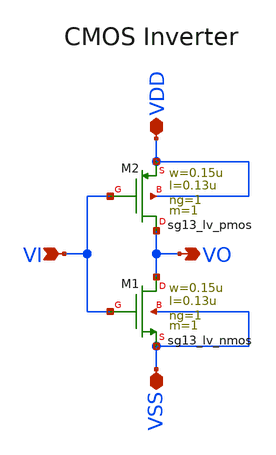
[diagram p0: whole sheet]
** sch_path: designs/archives/inv/inv.sch
**.subckt inv VDD VSS VI VO
*.iopin VDD
*.iopin VSS
*.ipin VI
*.opin VO
XM1 VO VI VSS VSS sg13_lv_nmos w=0.15u l=0.13u ng=1 m=1 mm_ok=1
XM2 VO VI VDD VDD sg13_lv_pmos w=0.15u l=0.13u ng=1 m=1 mm_ok=1
**.ends
.end
